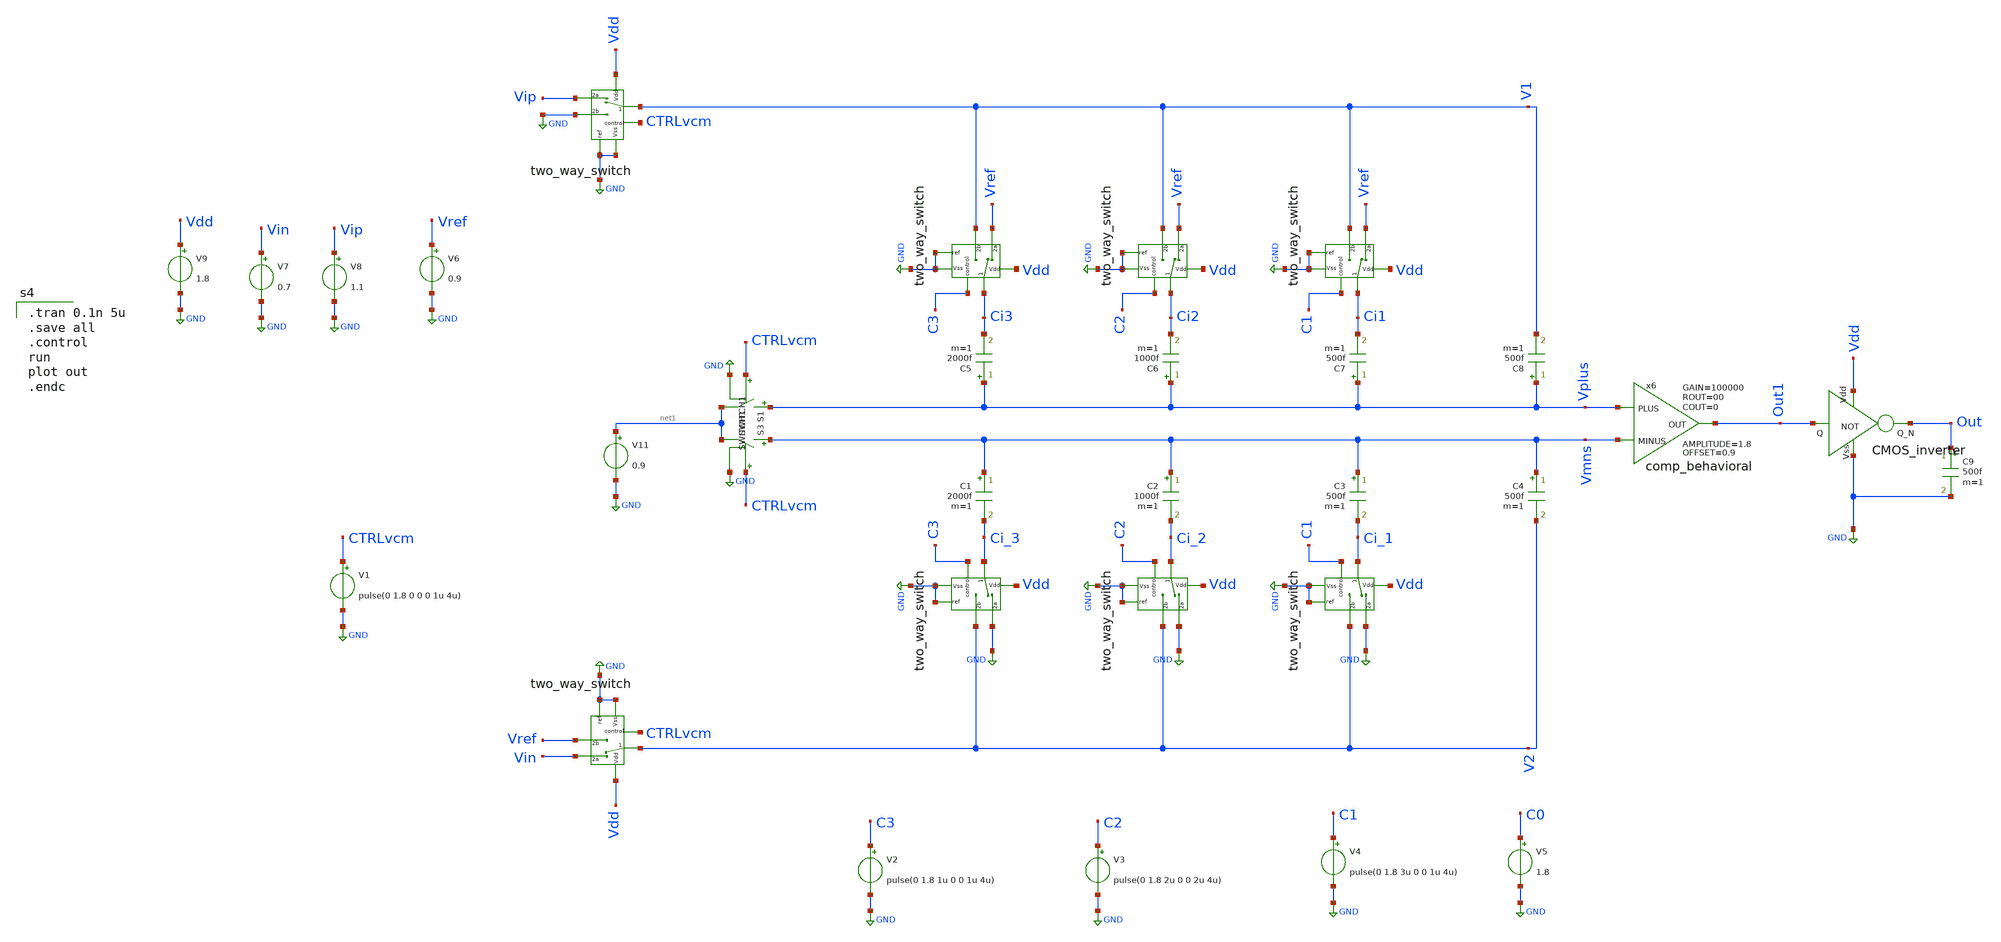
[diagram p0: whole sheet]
** sch_path: Behavioral_model/testing.sch
**.subckt testing
x6 Vplus Vmns Out1 comp_behavioral OFFSET=0.9 AMPLITUDE=1.8 GAIN=100000 ROUT=00 COUT=0
V11 net1 GND 0.9
C1 Vmns Ci_3 2000f m=1
C2 Vmns Ci_2 1000f m=1
C3 Vmns Ci_1 500f m=1
C4 Vmns V2 500f m=1
C5 Vplus Ci3 2000f m=1
C6 Vplus Ci2 1000f m=1
C7 Vplus Ci1 500f m=1
C8 Vplus V1 500f m=1
S1 Vplus net1 CTRLvcm GND SWITCH1
S3 Vmns net1 CTRLvcm GND SWITCH1
V1 CTRLvcm GND pulse(0 1.8 0 0 0 1u 4u)
x11 V1 Vdd CTRLvcm GND Vip GND GND two_way_switch
x5 Ci1 Vdd C1 GND Vref V1 GND two_way_switch
x7 Ci2 Vdd C2 GND Vref V1 GND two_way_switch
x8 Ci3 Vdd C3 GND Vref V1 GND two_way_switch
x2 V2 Vdd CTRLvcm GND Vin Vref GND two_way_switch
x3 Ci_1 Vdd C1 GND GND V2 GND two_way_switch
x4 Ci_2 Vdd C2 GND GND V2 GND two_way_switch
x10 Ci_3 Vdd C3 GND GND V2 GND two_way_switch
V6 Vref GND 0.9
V7 Vin GND 0.7
V8 Vip GND 1.1
V9 Vdd GND 1.8
V2 C3 GND pulse(0 1.8 1u 0 0 1u 4u)
V3 C2 GND pulse(0 1.8 2u 0 0 2u 4u)
V4 C1 GND pulse(0 1.8 3u 0 0 1u 4u)
V5 C0 GND 1.8
x12 Vdd Out1 Out GND CMOS_inverter
C9 Out GND 500f m=1
**** begin user architecture code

.lib /usr/local/share/pdk/sky130A/libs.tech/ngspice/sky130.lib.spice tt


.model switch1 sw vt=0.1 vh=0 ron=1m roff=100G


.tran 0.1n 5u
.save all
.control
run
plot out
.endc

**** end user architecture code
**.ends

* expanding   symbol:  comp_behavioral.sym # of pins=3
** sym_path: Behavioral_model/comp_behavioral.sym
** sch_path: Behavioral_model/comp_behavioral.sch
.subckt comp_behavioral PLUS MINUS OUT  OFFSET=0.9 AMPLITUDE=0.9 GAIN=100000 ROUT=00 COUT=0
*.ipin PLUS
*.ipin MINUS
*.opin OUT
B1 IOUT 0 V = {OFFSET + AMPLITUDE/2*(tanh(V(IPLUS,IMINUS)*GAIN*2/AMPLITUDE))}
V1 IPLUS PLUS 3
V2 IMINUS MINUS 3
R1 OUT IOUT {ROUT} m=1
C3 OUT 0 {COUT} m=1
.ends


* expanding   symbol:  two_way_switch.sym # of pins=7
** sym_path: Behavioral_model/two_way_switch.sym
** sch_path: Behavioral_model/two_way_switch.sch
.subckt two_way_switch 1 Vdd control ref 2a 2b Vss
*.iopin 2b
*.iopin 2a
*.ipin ref
*.iopin 1
*.ipin Vdd
*.ipin Vss
*.ipin control
S1 1 2a control ref SWITCH1
S2 1 2b net1 ref SWITCH1
x1 Vdd control net1 Vss CMOS_inverter
.ends


* expanding   symbol:  CMOS_inverter.sym # of pins=4
** sym_path: Behavioral_model/CMOS_inverter.sym
** sch_path: Behavioral_model/CMOS_inverter.sch
.subckt CMOS_inverter Vdd Q Q_N Vss
*.ipin Q
*.ipin Vdd
*.ipin Vss
*.opin Q_N
XM1 Q_N Q Vss Vss sky130_fd_pr__nfet_01v8 L=0.15 W=1 nf=1 ad='int((nf+1)/2) * W/nf * 0.29' as='int((nf+2)/2) * W/nf * 0.29'
+ pd='2*int((nf+1)/2) * (W/nf + 0.29)' ps='2*int((nf+2)/2) * (W/nf + 0.29)' nrd='0.29 / W' nrs='0.29 / W'
+ sa=0 sb=0 sd=0 mult=1 m=1
XM3 Q_N Q Vdd Vdd sky130_fd_pr__pfet_01v8 L=0.15 W=1 nf=1 ad='int((nf+1)/2) * W/nf * 0.29' as='int((nf+2)/2) * W/nf * 0.29'
+ pd='2*int((nf+1)/2) * (W/nf + 0.29)' ps='2*int((nf+2)/2) * (W/nf + 0.29)' nrd='0.29 / W' nrs='0.29 / W'
+ sa=0 sb=0 sd=0 mult=1 m=1
.ends

.GLOBAL GND
.end
